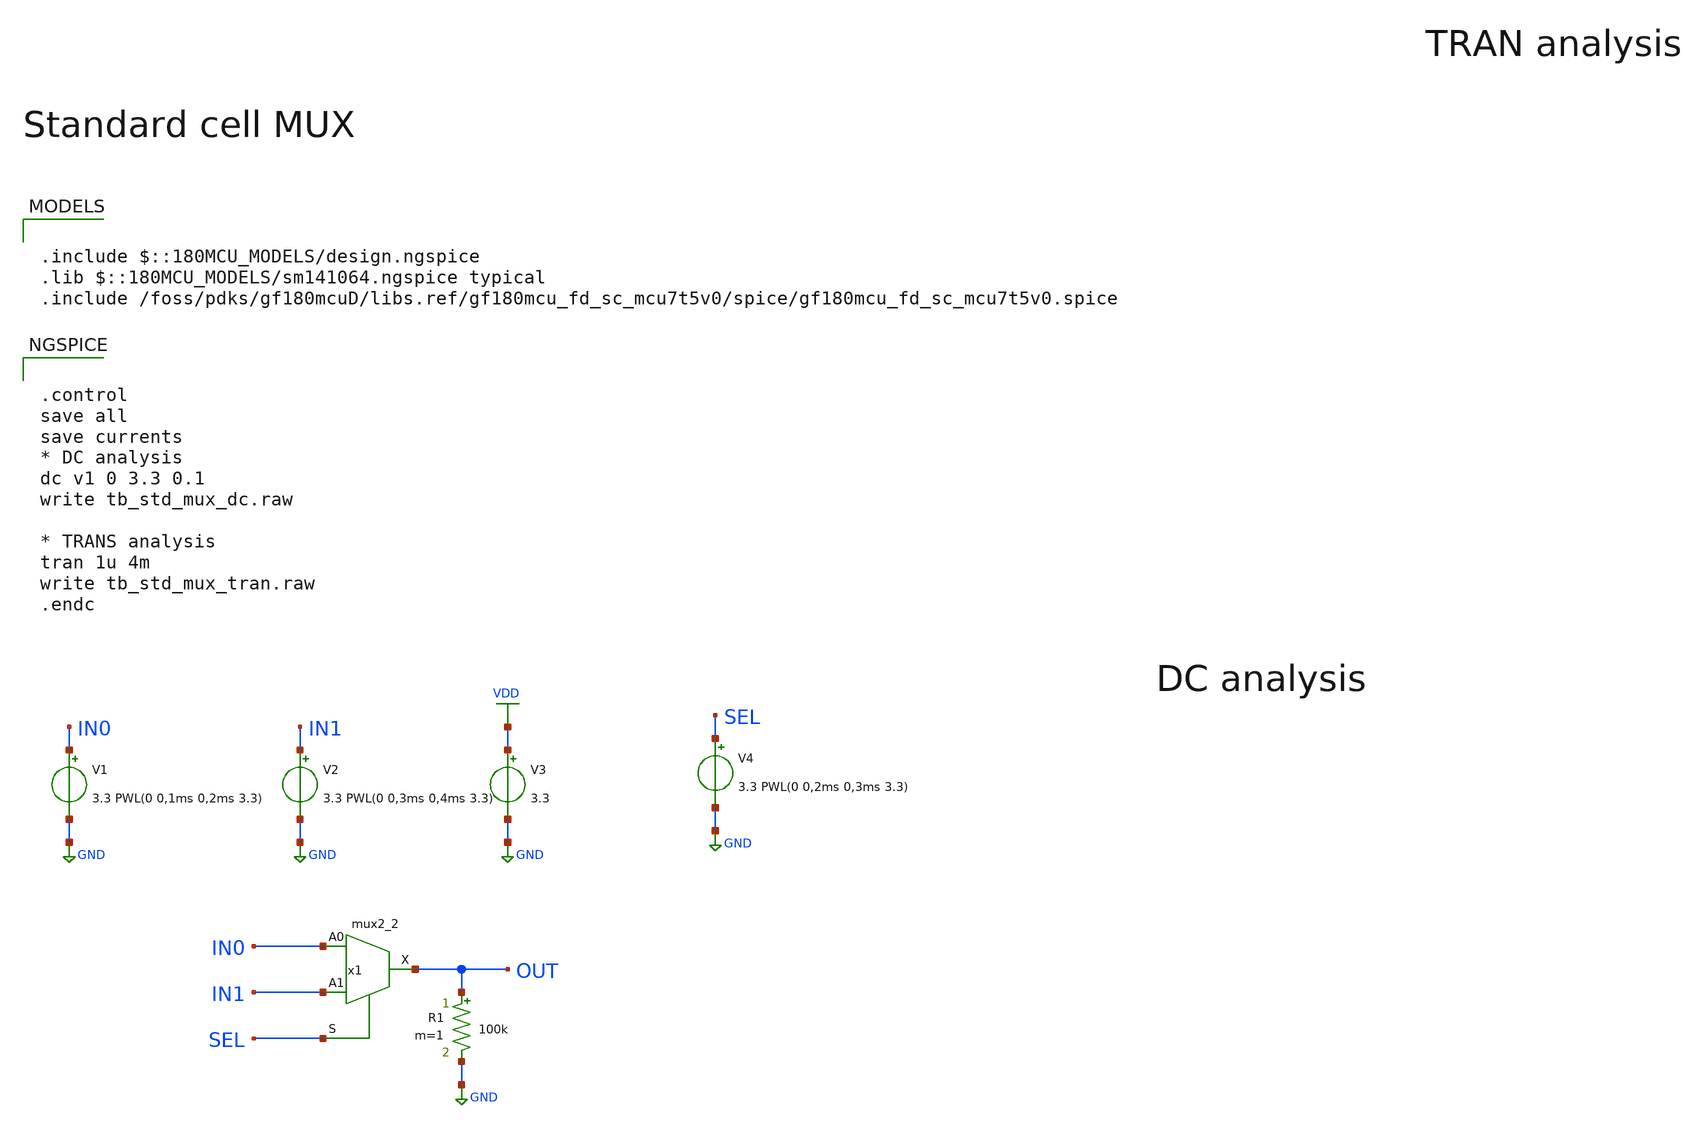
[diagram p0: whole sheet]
** sch_path: designs/libs/tb_analog/tb_std_mux/tb_std_mux.sch
* Copyright 2022 GlobalFoundries PDK Authors
* Licensed under the Apache License, Version 2.0 (the "License");
* you may not use this file except in compliance with the License.
* You may obtain a copy of the License at
* https://www.apache.org/licenses/LICENSE-2.0
* Unless required by applicable law or agreed to in writing, software
* distributed under the License is distributed on an "AS IS" BASIS,
* WITHOUT WARRANTIES OR CONDITIONS OF ANY KIND, either express or implied.
* See the License for the specific language governing permissions and
* limitations under the License.
**.subckt tb_std_mux
V1 IN0 GND 3.3 PWL(0 0,1ms 0,2ms 3.3)
V2 IN1 GND 3.3 PWL(0 0,3ms 0,4ms 3.3)
V3 VDD GND 3.3
R1 OUT GND 100k m=1
V4 SEL GND 3.3 PWL(0 0,2ms 0,3ms 3.3)
x1 IN0 IN1 SEL OUT VDD VDD GND GND gf180mcu_fd_sc_mcu7t5v0__mux2_2
**** begin user architecture code

.include $::180MCU_MODELS/design.ngspice
.lib $::180MCU_MODELS/sm141064.ngspice typical
.include /foss/pdks/gf180mcuD/libs.ref/gf180mcu_fd_sc_mcu7t5v0/spice/gf180mcu_fd_sc_mcu7t5v0.spice




.control
save all
save currents
* DC analysis
dc v1 0 3.3 0.1
write tb_std_mux_dc.raw

* TRANS analysis
tran 1u 4m
write tb_std_mux_tran.raw
.endc


**** end user architecture code
**.ends
.GLOBAL VDD
.GLOBAL GND
.end
